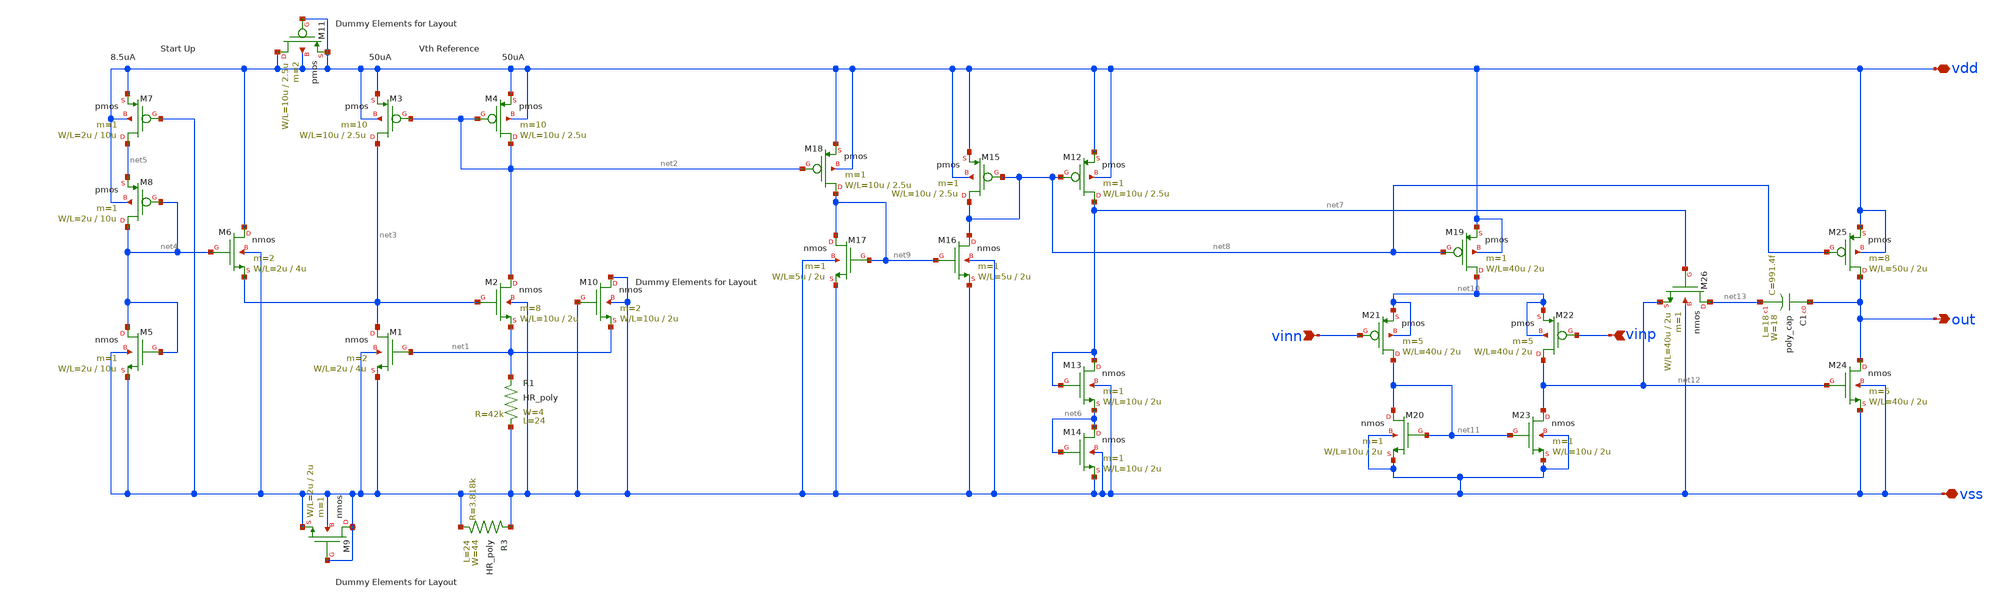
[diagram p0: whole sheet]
** sch_path: member_project/GroupWork/Team_Ando/ugeugeHigh/opamp_cs_full.sch
**.subckt opamp_cs_full vss vinn vinp out vdd
*.iopin vss
*.ipin vinn
*.ipin vinp
*.opin out
*.iopin vdd
R1 vss net1 HR_poly W=4 L=24
M1 net3 net1 vss vss nmos L=4u W=2u m=2
M2 net2 net3 net1 vss nmos L=2u W=10u m=8
M3 net3 net2 vdd vdd pmos L=2.5u W=10u m=10
M4 net2 net2 vdd vdd pmos L=2.5u W=10u m=10
M5 net4 net4 vss vss nmos L=10u W=2u m=1
M6 vdd net4 net3 vss nmos L=4u W=2u m=2
M7 net5 vss vdd vdd pmos L=10u W=2u m=1
M8 net4 net4 net5 vdd pmos L=10u W=2u m=1
R3 vss vss HR_poly W=44 L=24
M9 vss vss vss vss nmos L=2u W=2u m=1
M10 vss vss net1 vss nmos L=2u W=10u m=2
M11 vdd vdd vdd vdd pmos L=2.5u W=10u m=2
M12 net7 net8 vdd vdd pmos L=2.5u W=10u m=1
M13 net7 net7 net6 vss nmos L=2u W=10u m=1
M14 net6 net6 vss vss nmos L=2u W=10u m=1
M15 net8 net8 vdd vdd pmos L=2.5u W=10u m=1
M16 net8 net9 vss vss nmos L=2u W=5u m=1
M17 net9 net9 vss vss nmos L=2u W=5u m=1
M18 net9 net2 vdd vdd pmos L=2.5u W=10u m=1
M19 net10 net8 vdd vdd pmos L=2u W=40u m=1
M20 net11 net11 vss vss nmos L=2u W=10u m=1
M21 net11 vinn net10 net10 pmos L=2u W=40u m=5
M22 net12 vinp net10 net10 pmos L=2u W=40u m=5
M23 net12 net11 vss vss nmos L=2u W=10u m=1
M24 out net12 vss vss nmos L=2u W=40u m=5
M25 out net8 vdd vdd pmos L=2u W=50u m=8
M26 net13 net7 net12 vss nmos L=2u W=40u m=1
C1 out net13 poly_cap W=18 L=18
**.ends
.end
